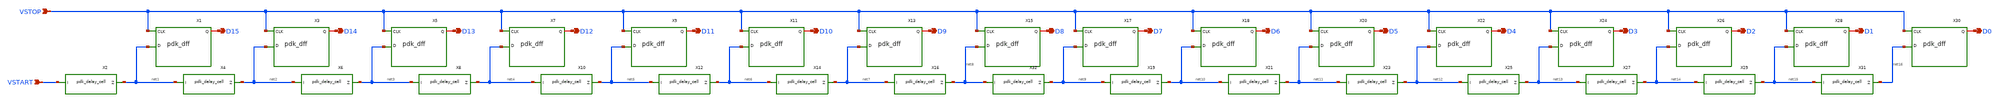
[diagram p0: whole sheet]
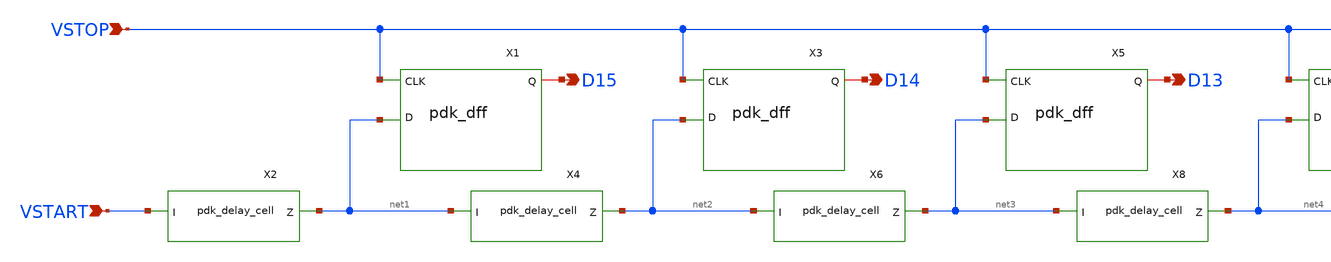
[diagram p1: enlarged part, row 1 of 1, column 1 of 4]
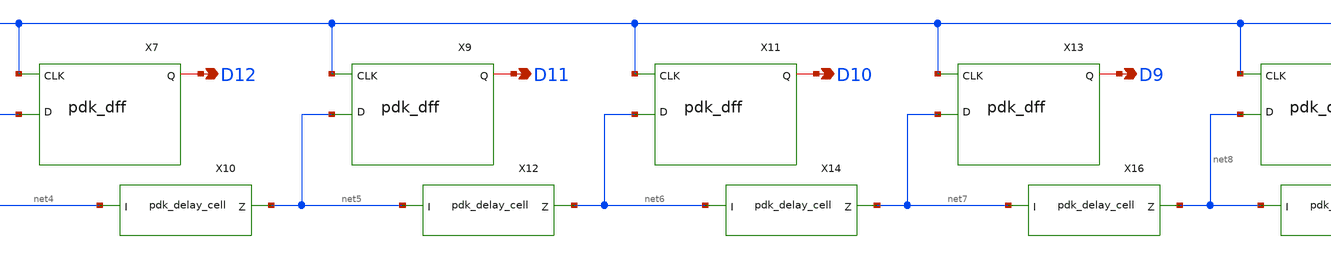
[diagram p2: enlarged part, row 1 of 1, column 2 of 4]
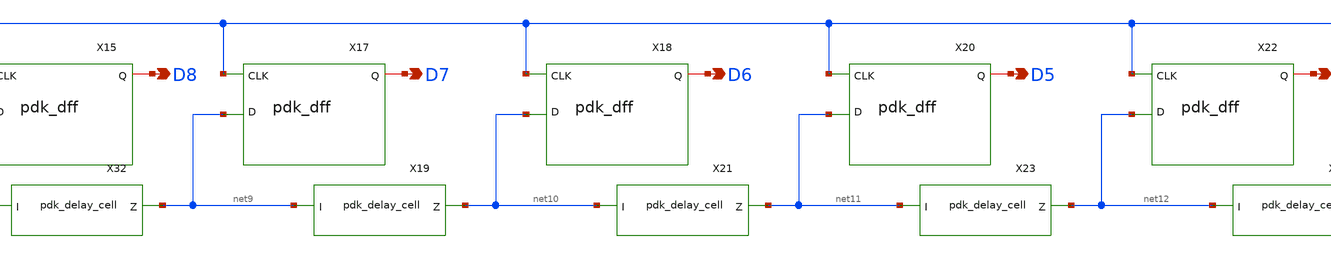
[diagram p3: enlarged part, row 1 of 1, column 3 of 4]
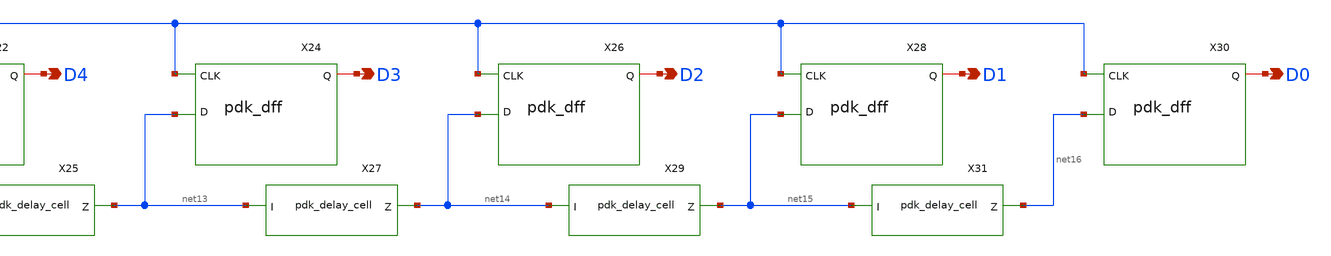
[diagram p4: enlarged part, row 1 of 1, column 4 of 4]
** sch_path: schem/medium_delay_line.sch
**.subckt medium_delay_line VSTOP VSTART D15 D14 D13 D12 D11 D10 D9 D8 D7 D6 D5 D4 D3 D2 D1 D0
*.ipin VSTOP
*.ipin VSTART
*.opin D15
*.opin D14
*.opin D13
*.opin D12
*.opin D11
*.opin D10
*.opin D9
*.opin D8
*.opin D7
*.opin D6
*.opin D5
*.opin D4
*.opin D3
*.opin D2
*.opin D1
*.opin D0
X1 net1 VSTOP D15 VDD VDD 0 0 gf180mcu_fd_sc_mcu7t5v0__dffq_1
X2 VSTART net1 VDD VDD 0 0 gf180mcu_fd_sc_mcu7t5v0__dlyc_1
X3 net2 VSTOP D14 VDD VDD 0 0 gf180mcu_fd_sc_mcu7t5v0__dffq_1
X4 net1 net2 VDD VDD 0 0 gf180mcu_fd_sc_mcu7t5v0__dlyc_1
X5 net3 VSTOP D13 VDD VDD 0 0 gf180mcu_fd_sc_mcu7t5v0__dffq_1
X6 net2 net3 VDD VDD 0 0 gf180mcu_fd_sc_mcu7t5v0__dlyc_1
X7 net4 VSTOP D12 VDD VDD 0 0 gf180mcu_fd_sc_mcu7t5v0__dffq_1
X8 net3 net4 VDD VDD 0 0 gf180mcu_fd_sc_mcu7t5v0__dlyc_1
X9 net5 VSTOP D11 VDD VDD 0 0 gf180mcu_fd_sc_mcu7t5v0__dffq_1
X10 net4 net5 VDD VDD 0 0 gf180mcu_fd_sc_mcu7t5v0__dlyc_1
X11 net6 VSTOP D10 VDD VDD 0 0 gf180mcu_fd_sc_mcu7t5v0__dffq_1
X12 net5 net6 VDD VDD 0 0 gf180mcu_fd_sc_mcu7t5v0__dlyc_1
X13 net7 VSTOP D9 VDD VDD 0 0 gf180mcu_fd_sc_mcu7t5v0__dffq_1
X14 net6 net7 VDD VDD 0 0 gf180mcu_fd_sc_mcu7t5v0__dlyc_1
X15 net8 VSTOP D8 VDD VDD 0 0 gf180mcu_fd_sc_mcu7t5v0__dffq_1
X16 net7 net8 VDD VDD 0 0 gf180mcu_fd_sc_mcu7t5v0__dlyc_1
X17 net9 VSTOP D7 VDD VDD 0 0 gf180mcu_fd_sc_mcu7t5v0__dffq_1
X18 net10 VSTOP D6 VDD VDD 0 0 gf180mcu_fd_sc_mcu7t5v0__dffq_1
X19 net9 net10 VDD VDD 0 0 gf180mcu_fd_sc_mcu7t5v0__dlyc_1
X20 net11 VSTOP D5 VDD VDD 0 0 gf180mcu_fd_sc_mcu7t5v0__dffq_1
X21 net10 net11 VDD VDD 0 0 gf180mcu_fd_sc_mcu7t5v0__dlyc_1
X22 net12 VSTOP D4 VDD VDD 0 0 gf180mcu_fd_sc_mcu7t5v0__dffq_1
X23 net11 net12 VDD VDD 0 0 gf180mcu_fd_sc_mcu7t5v0__dlyc_1
X24 net13 VSTOP D3 VDD VDD 0 0 gf180mcu_fd_sc_mcu7t5v0__dffq_1
X25 net12 net13 VDD VDD 0 0 gf180mcu_fd_sc_mcu7t5v0__dlyc_1
X26 net14 VSTOP D2 VDD VDD 0 0 gf180mcu_fd_sc_mcu7t5v0__dffq_1
X27 net13 net14 VDD VDD 0 0 gf180mcu_fd_sc_mcu7t5v0__dlyc_1
X28 net15 VSTOP D1 VDD VDD 0 0 gf180mcu_fd_sc_mcu7t5v0__dffq_1
X29 net14 net15 VDD VDD 0 0 gf180mcu_fd_sc_mcu7t5v0__dlyc_1
X30 net16 VSTOP D0 VDD VDD 0 0 gf180mcu_fd_sc_mcu7t5v0__dffq_1
X31 net15 net16 VDD VDD 0 0 gf180mcu_fd_sc_mcu7t5v0__dlyc_1
X32 net8 net9 VDD VDD 0 0 gf180mcu_fd_sc_mcu7t5v0__dlyc_1
**.ends
.end
